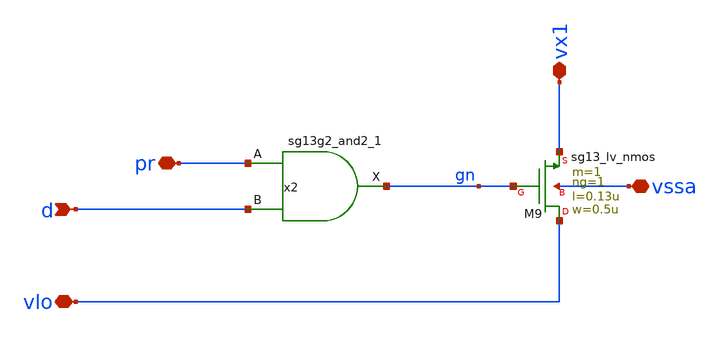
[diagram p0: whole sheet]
** sch_path: 5_Design/4_Layout/Team 5/xschem/integ_5_split2.2.sch
**.subckt integ_5_split2.2 d vlo pr vx1 vssa
*.ipin d
*.iopin vlo
*.iopin pr
*.iopin vx1
*.iopin vssa
XM9 vlo gn vx1 vssa sg13_lv_nmos w=0.5u l=0.13u ng=1 m=1 mm_ok=1
x2 gn pr d VDD VSS sg13g2_and2_1
**.ends

* expanding   symbol:  sg13g2_stdcells/sg13g2_and2_1.sym # of pins=3
** sym_path: sg13g2_stdcells/sg13g2_and2_1.sym
** sch_path: sg13g2_stdcells/sg13g2_and2_1.sch
.subckt sg13g2_and2_1 X A B VDD VSS
*.ipin A
*.ipin B
*.opin X
*.iopin VDD
*.iopin VSS
XM1 net1 A net2 VSS sg13_lv_nmos w=640.00n l=130.00n ng=1 m=1 mm_ok=1
XM2 net2 B VSS VSS sg13_lv_nmos w=640.00n l=130.00n ng=1 m=1 mm_ok=1
XM3 X net1 VSS VSS sg13_lv_nmos w=740.00n l=130.00n ng=1 m=1 mm_ok=1
XM4 net1 B VDD VDD sg13_lv_pmos w=840.00n l=130.00n ng=1 m=1 mm_ok=1
XM5 net1 A VDD VDD sg13_lv_pmos w=840.00n l=130.00n ng=1 m=1 mm_ok=1
XM6 X net1 VDD VDD sg13_lv_pmos w=1.12u l=130.00n ng=1 m=1 mm_ok=1
.ends

.end
